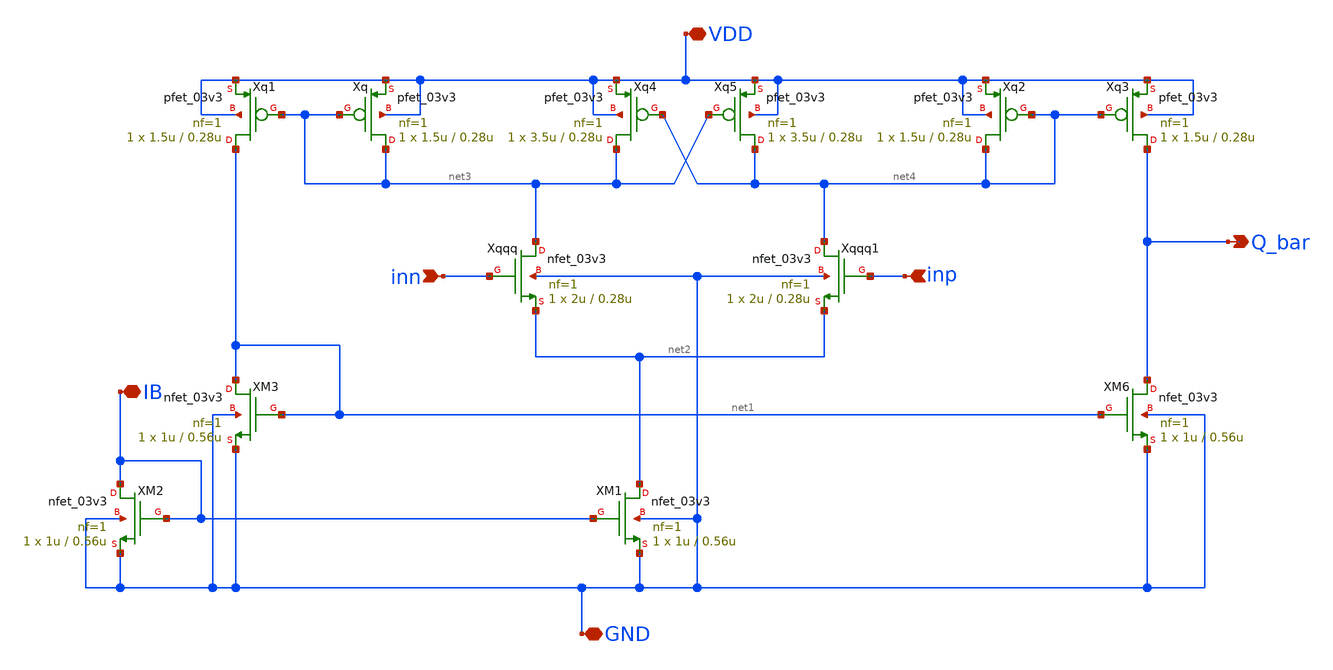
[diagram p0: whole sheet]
** sch_path: analog/B04_comparator.sch
**.subckt B04_comparator VDD GND inn inp IB Q_bar
*.iopin VDD
*.iopin GND
*.ipin inn
*.ipin inp
*.iopin IB
*.opin Q_bar
XM1 net2 IB GND GND nfet_03v3 L=0.56u W=1u nf=1 ad='int((nf+1)/2) * W/nf * 0.18u' as='int((nf+2)/2) * W/nf * 0.18u'
+ pd='2*int((nf+1)/2) * (W/nf + 0.18u)' ps='2*int((nf+2)/2) * (W/nf + 0.18u)' nrd='0.18u / W' nrs='0.18u / W'
+ sa=0 sb=0 sd=0 m=1
XM2 IB IB GND GND nfet_03v3 L=0.56u W=1u nf=1 ad='int((nf+1)/2) * W/nf * 0.18u' as='int((nf+2)/2) * W/nf * 0.18u'
+ pd='2*int((nf+1)/2) * (W/nf + 0.18u)' ps='2*int((nf+2)/2) * (W/nf + 0.18u)' nrd='0.18u / W' nrs='0.18u / W'
+ sa=0 sb=0 sd=0 m=1
XM3 net1 net1 GND GND nfet_03v3 L=0.56u W=1u nf=1 ad='int((nf+1)/2) * W/nf * 0.18u' as='int((nf+2)/2) * W/nf * 0.18u'
+ pd='2*int((nf+1)/2) * (W/nf + 0.18u)' ps='2*int((nf+2)/2) * (W/nf + 0.18u)' nrd='0.18u / W' nrs='0.18u / W'
+ sa=0 sb=0 sd=0 m=1
Xqqq net3 inn net2 GND nfet_03v3 L=0.28u W=2u nf=1 ad='int((nf+1)/2) * W/nf * 0.18u' as='int((nf+2)/2) * W/nf * 0.18u'
+ pd='2*int((nf+1)/2) * (W/nf + 0.18u)' ps='2*int((nf+2)/2) * (W/nf + 0.18u)' nrd='0.18u / W' nrs='0.18u / W'
+ sa=0 sb=0 sd=0 m=1
Xqqq1 net4 inp net2 GND nfet_03v3 L=0.28u W=2u nf=1 ad='int((nf+1)/2) * W/nf * 0.18u' as='int((nf+2)/2) * W/nf * 0.18u'
+ pd='2*int((nf+1)/2) * (W/nf + 0.18u)' ps='2*int((nf+2)/2) * (W/nf + 0.18u)' nrd='0.18u / W' nrs='0.18u / W'
+ sa=0 sb=0 sd=0 m=1
XM6 Q_bar net1 GND GND nfet_03v3 L=0.56u W=1u nf=1 ad='int((nf+1)/2) * W/nf * 0.18u' as='int((nf+2)/2) * W/nf * 0.18u'
+ pd='2*int((nf+1)/2) * (W/nf + 0.18u)' ps='2*int((nf+2)/2) * (W/nf + 0.18u)' nrd='0.18u / W' nrs='0.18u / W'
+ sa=0 sb=0 sd=0 m=1
Xq net3 net3 VDD VDD pfet_03v3 L=0.28u W=1.5u nf=1 ad='int((nf+1)/2) * W/nf * 0.18u' as='int((nf+2)/2) * W/nf * 0.18u'
+ pd='2*int((nf+1)/2) * (W/nf + 0.18u)' ps='2*int((nf+2)/2) * (W/nf + 0.18u)' nrd='0.18u / W' nrs='0.18u / W'
+ sa=0 sb=0 sd=0 m=1
Xq1 net1 net3 VDD VDD pfet_03v3 L=0.28u W=1.5u nf=1 ad='int((nf+1)/2) * W/nf * 0.18u' as='int((nf+2)/2) * W/nf * 0.18u'
+ pd='2*int((nf+1)/2) * (W/nf + 0.18u)' ps='2*int((nf+2)/2) * (W/nf + 0.18u)' nrd='0.18u / W' nrs='0.18u / W'
+ sa=0 sb=0 sd=0 m=1
Xq4 net3 net4 VDD VDD pfet_03v3 L=0.28u W=3.5u nf=1 ad='int((nf+1)/2) * W/nf * 0.18u' as='int((nf+2)/2) * W/nf * 0.18u'
+ pd='2*int((nf+1)/2) * (W/nf + 0.18u)' ps='2*int((nf+2)/2) * (W/nf + 0.18u)' nrd='0.18u / W' nrs='0.18u / W'
+ sa=0 sb=0 sd=0 m=1
Xq5 net4 net3 VDD VDD pfet_03v3 L=0.28u W=3.5u nf=1 ad='int((nf+1)/2) * W/nf * 0.18u' as='int((nf+2)/2) * W/nf * 0.18u'
+ pd='2*int((nf+1)/2) * (W/nf + 0.18u)' ps='2*int((nf+2)/2) * (W/nf + 0.18u)' nrd='0.18u / W' nrs='0.18u / W'
+ sa=0 sb=0 sd=0 m=1
Xq2 net4 net4 VDD VDD pfet_03v3 L=0.28u W=1.5u nf=1 ad='int((nf+1)/2) * W/nf * 0.18u' as='int((nf+2)/2) * W/nf * 0.18u'
+ pd='2*int((nf+1)/2) * (W/nf + 0.18u)' ps='2*int((nf+2)/2) * (W/nf + 0.18u)' nrd='0.18u / W' nrs='0.18u / W'
+ sa=0 sb=0 sd=0 m=1
Xq3 Q_bar net4 VDD VDD pfet_03v3 L=0.28u W=1.5u nf=1 ad='int((nf+1)/2) * W/nf * 0.18u' as='int((nf+2)/2) * W/nf * 0.18u'
+ pd='2*int((nf+1)/2) * (W/nf + 0.18u)' ps='2*int((nf+2)/2) * (W/nf + 0.18u)' nrd='0.18u / W' nrs='0.18u / W'
+ sa=0 sb=0 sd=0 m=1
**.ends
.end
